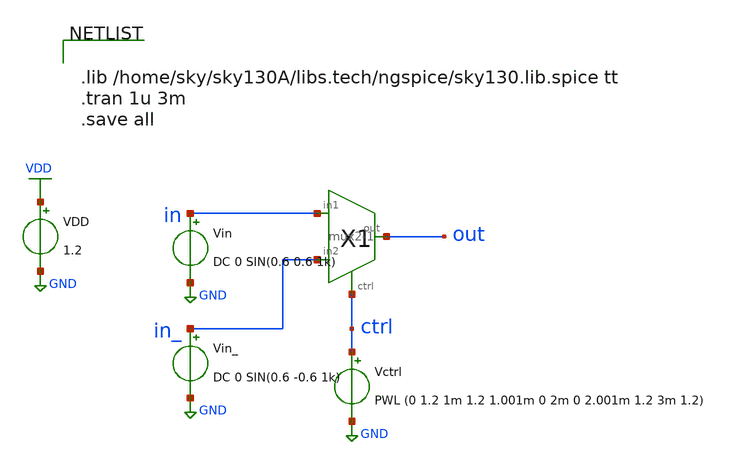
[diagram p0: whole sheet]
** sch_path: xschem/mux/mux2-1_tb.sch
**.subckt mux2-1_tb
Vin in GND DC 0 SIN(0.6 0.6 1k)
VDD VDD GND 1.2
Vctrl ctrl GND PWL (0 1.2 1m 1.2 1.001m 0 2m 0 2.001m 1.2 3m 1.2)
X1 in out in_ ctrl mux2-1
Vin_ in_ GND DC 0 SIN(0.6 -0.6 1k)
**** begin user architecture code


.lib /home/sky/sky130A/libs.tech/ngspice/sky130.lib.spice tt
.tran 1u 3m
.save all


**** end user architecture code
**.ends

* expanding   symbol:  mux/mux2-1.sym # of pins=4
** sym_path: xschem/mux/mux2-1.sym
** sch_path: xschem/mux/mux2-1.sch
.subckt mux2-1 in1 out in2 ctrl
*.ipin in1
*.ipin ctrl
*.ipin in2
*.iopin out
X1 in1 out net1 ctrl transmission_gate Wpmos=3 Lpmos=0.18 Wnmos=1 Lnmos=0.18
X2 in2 out ctrl net1 transmission_gate Wpmos=3 Lpmos=0.18 Wnmos=1 Lnmos=0.18
X4 ctrl net1 inv Wpmos=3 Lpmos=0.18 Wnmos=1 Lnmos=0.18
.ends


* expanding   symbol:  transmission_gate/transmission_gate.sym # of pins=4
** sym_path: xschem/transmission_gate/transmission_gate.sym
** sch_path: xschem/transmission_gate/transmission_gate.sch
.subckt transmission_gate in out ctrl_ ctrl  Wpmos=1 Lpmos=0.18 Wnmos=1 Lnmos=0.18
*.iopin in
*.iopin out
*.ipin ctrl_
*.ipin ctrl
XM1 in ctrl out GND sky130_fd_pr__nfet_01v8 L=Lnmos W=Wnmos nf=1 ad='int((nf+1)/2) * W/nf * 0.29' as='int((nf+2)/2) * W/nf * 0.29'
+ pd='2*int((nf+1)/2) * (W/nf + 0.29)' ps='2*int((nf+2)/2) * (W/nf + 0.29)' nrd='0.29 / W' nrs='0.29 / W'
+ sa=0 sb=0 sd=0 mult=1 m=1
XM2 out ctrl_ in VDD sky130_fd_pr__pfet_01v8 L=Lpmos W=Wpmos nf=1 ad='int((nf+1)/2) * W/nf * 0.29' as='int((nf+2)/2) * W/nf * 0.29'
+ pd='2*int((nf+1)/2) * (W/nf + 0.29)' ps='2*int((nf+2)/2) * (W/nf + 0.29)' nrd='0.29 / W' nrs='0.29 / W'
+ sa=0 sb=0 sd=0 mult=1 m=1
.ends


* expanding   symbol:  inv/inv.sym # of pins=2
** sym_path: xschem/inv/inv.sym
** sch_path: xschem/inv/inv.sch
.subckt inv in out  Wpmos=3 Lpmos=0.18 Wnmos=1 Lnmos=0.18
*.ipin in
*.iopin out
XM1 out in GND GND sky130_fd_pr__nfet_01v8 L=Lnmos W=Wnmos nf=1 ad='int((nf+1)/2) * W/nf * 0.29' as='int((nf+2)/2) * W/nf * 0.29'
+ pd='2*int((nf+1)/2) * (W/nf + 0.29)' ps='2*int((nf+2)/2) * (W/nf + 0.29)' nrd='0.29 / W' nrs='0.29 / W'
+ sa=0 sb=0 sd=0 mult=1 m=1
XM2 out in VDD VDD sky130_fd_pr__pfet_01v8 L=Lpmos W=Wpmos nf=1 ad='int((nf+1)/2) * W/nf * 0.29' as='int((nf+2)/2) * W/nf * 0.29'
+ pd='2*int((nf+1)/2) * (W/nf + 0.29)' ps='2*int((nf+2)/2) * (W/nf + 0.29)' nrd='0.29 / W' nrs='0.29 / W'
+ sa=0 sb=0 sd=0 mult=1 m=1
.ends

.GLOBAL VDD
.GLOBAL GND
.end
